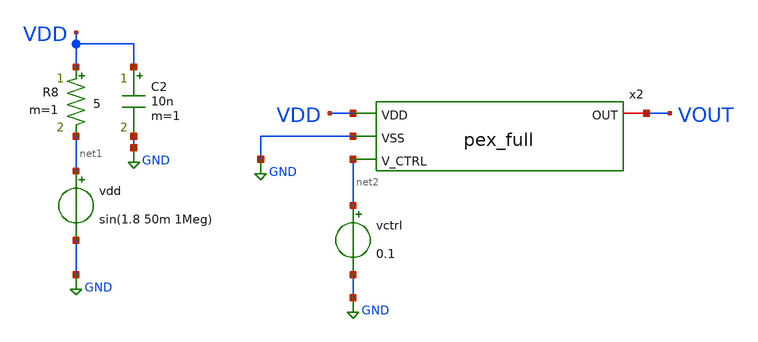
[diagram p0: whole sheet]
** sch_path: schem/voltage_full_tb.sch
**.subckt voltage_full_tb
vdd net1 GND sin(1.8 50m 1Meg)
C2 VDD GND 10n m=1
R8 VDD net1 5 m=1
vctrl net2 GND 0.1
x2 VDD GND VOUT net2 vco_pex
**** begin user architecture code


.include /home/zhixuan/projects/fyp_vco/magic/full/vco_pex.spice
.lib /usr/local/share/pdk/sky130A/libs.tech/ngspice/sky130.lib.spice tt
.save all

.control
    tran 0.1n 10u
    plot VOUT

    * Save VDD and VOUT to file for MATLAB
    echo "time,vdd,vout" > /home/zhixuan/projects/fyp_vco/schem/noise_out.txt
    print col time v(vdd) VOUT >> /home/zhixuan/projects/fyp_vco/schem/noise_out.txt

.endc

* VDD with 50mV 1MHz sinusoidal ripple on top of 1.8V DC

.end


**** end user architecture code
**.ends
.GLOBAL GND
.end
